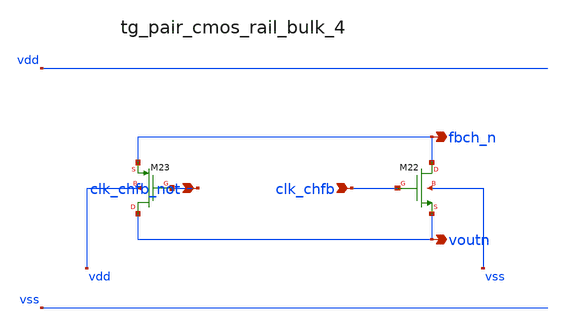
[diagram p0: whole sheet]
** sch_path: analog-db/raw/ia_002_fan_chopper_simple/hier/blocks/tg_pair_cmos_rail_bulk_4.sch
**.subckt tg_pair_cmos_rail_bulk_4 clk_chfb_not clk_chfb fbch_n voutn
*.ipin clk_chfb_not
*.ipin clk_chfb
*.opin fbch_n
*.opin voutn
XM22 fbch_n clk_chfb voutn vss sg13_lv_nmos w=x_dut_xm22_w l=x_dut_xm22_l ng=1 m=x_dut_xm22_m
XM23 voutn clk_chfb_not fbch_n vdd sg13_lv_pmos w=x_dut_xm23_w l=x_dut_xm23_l ng=1 m=x_dut_xm23_m
**.ends
.end
